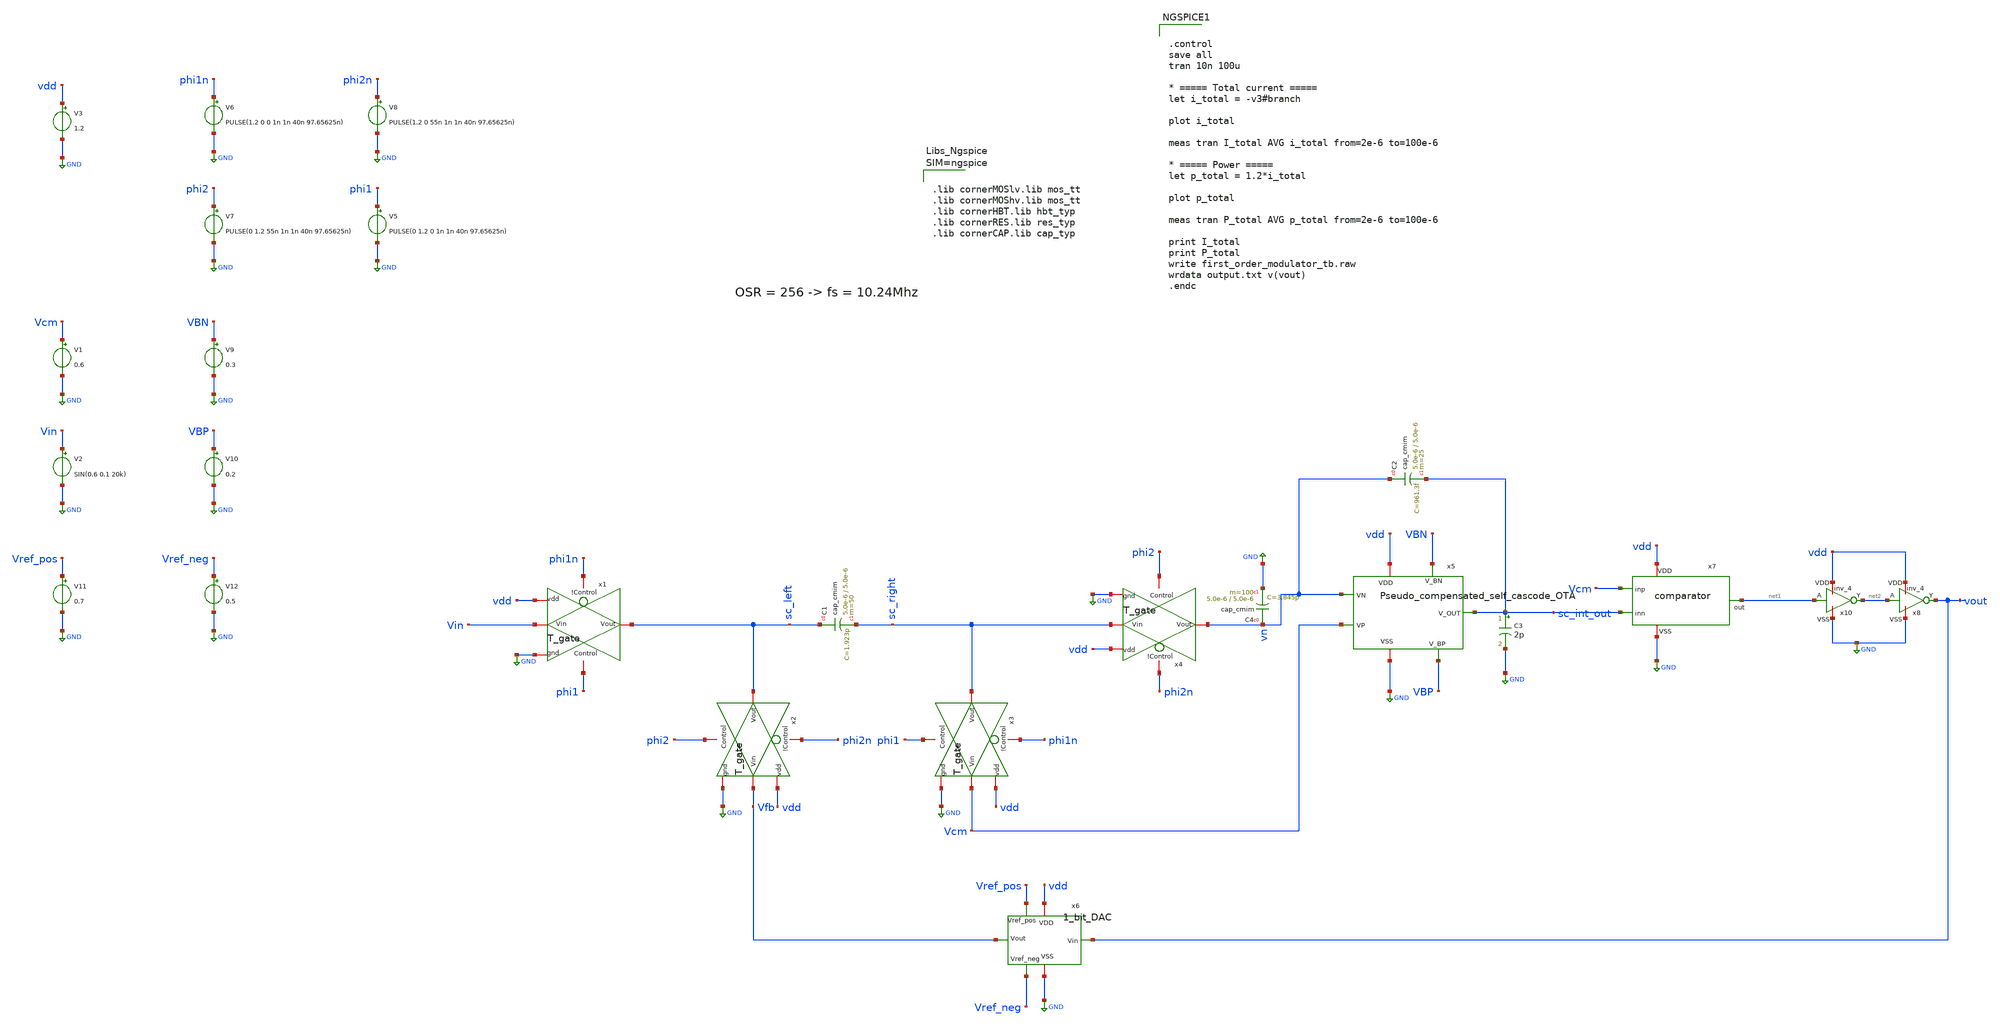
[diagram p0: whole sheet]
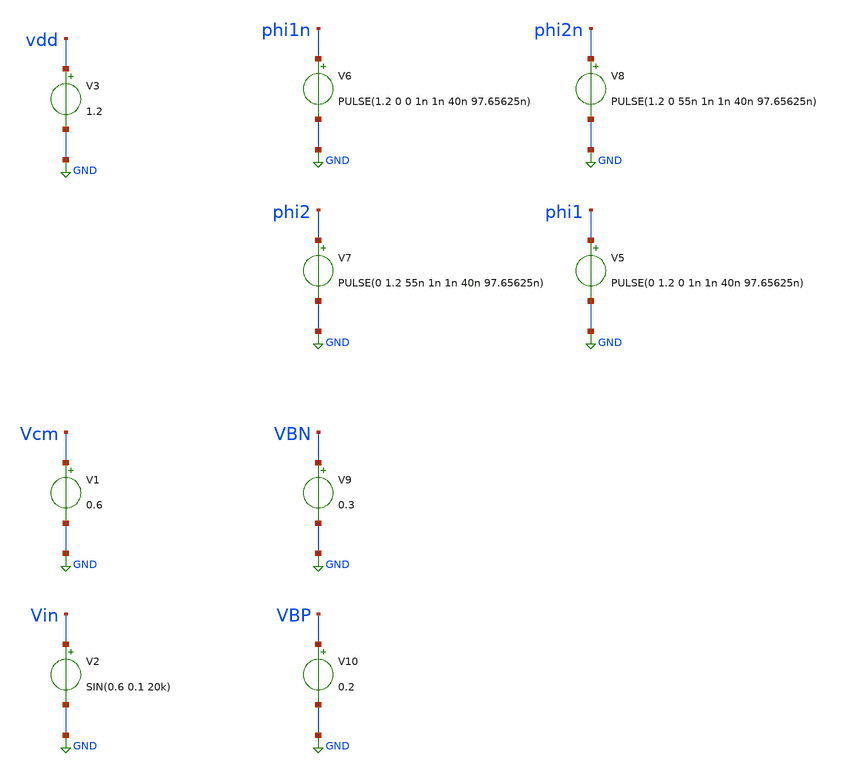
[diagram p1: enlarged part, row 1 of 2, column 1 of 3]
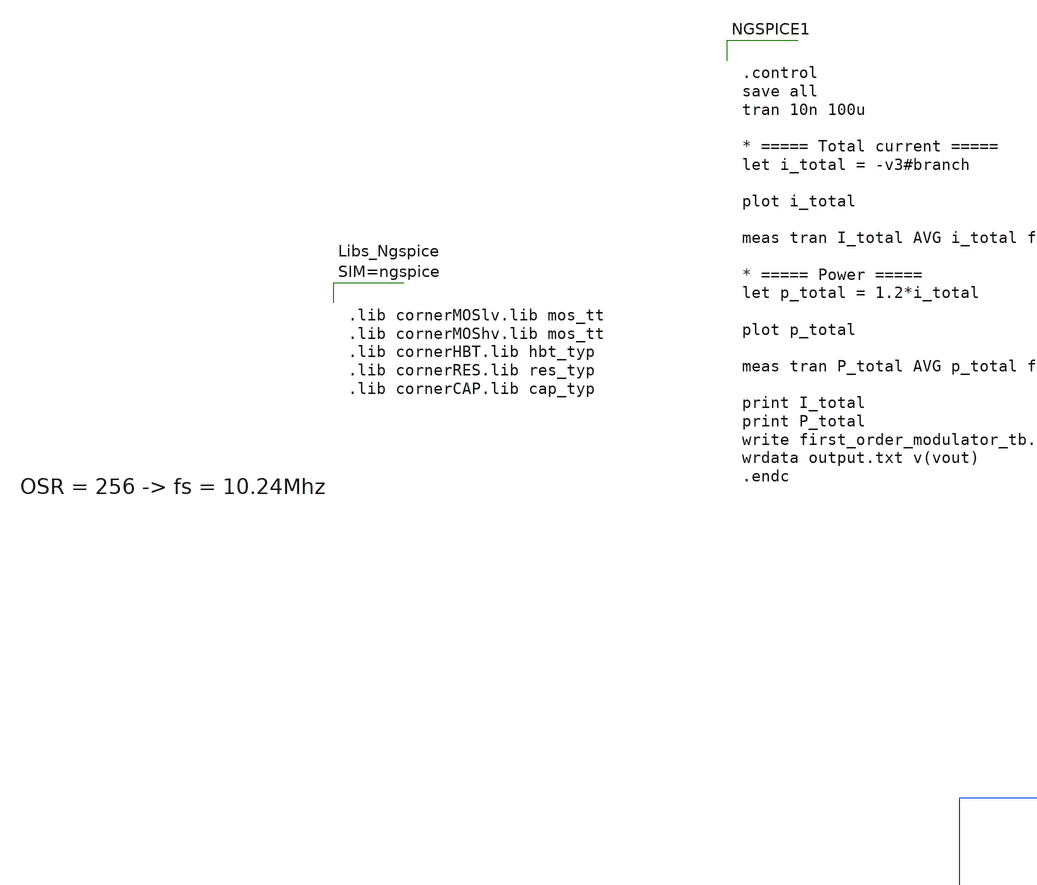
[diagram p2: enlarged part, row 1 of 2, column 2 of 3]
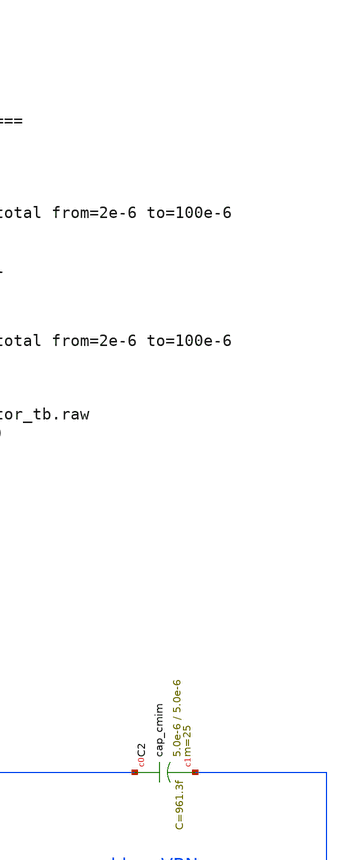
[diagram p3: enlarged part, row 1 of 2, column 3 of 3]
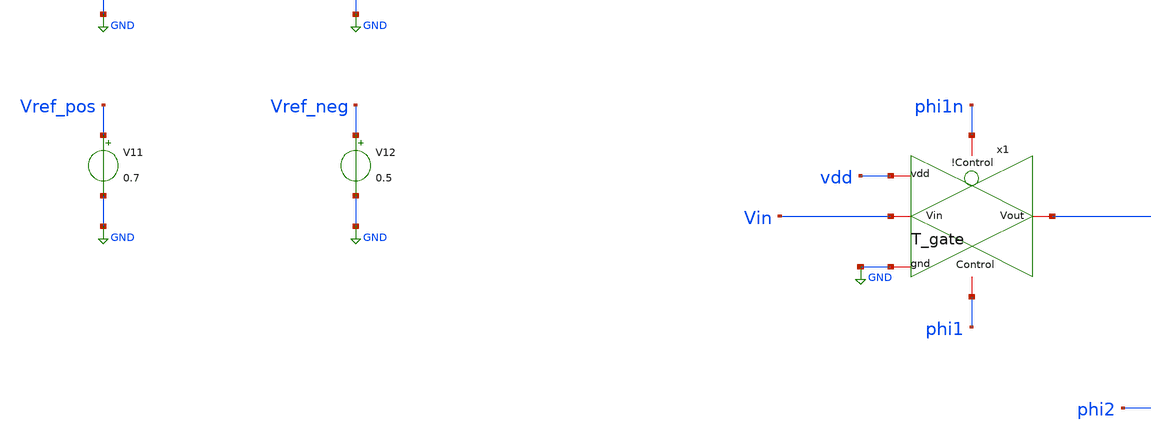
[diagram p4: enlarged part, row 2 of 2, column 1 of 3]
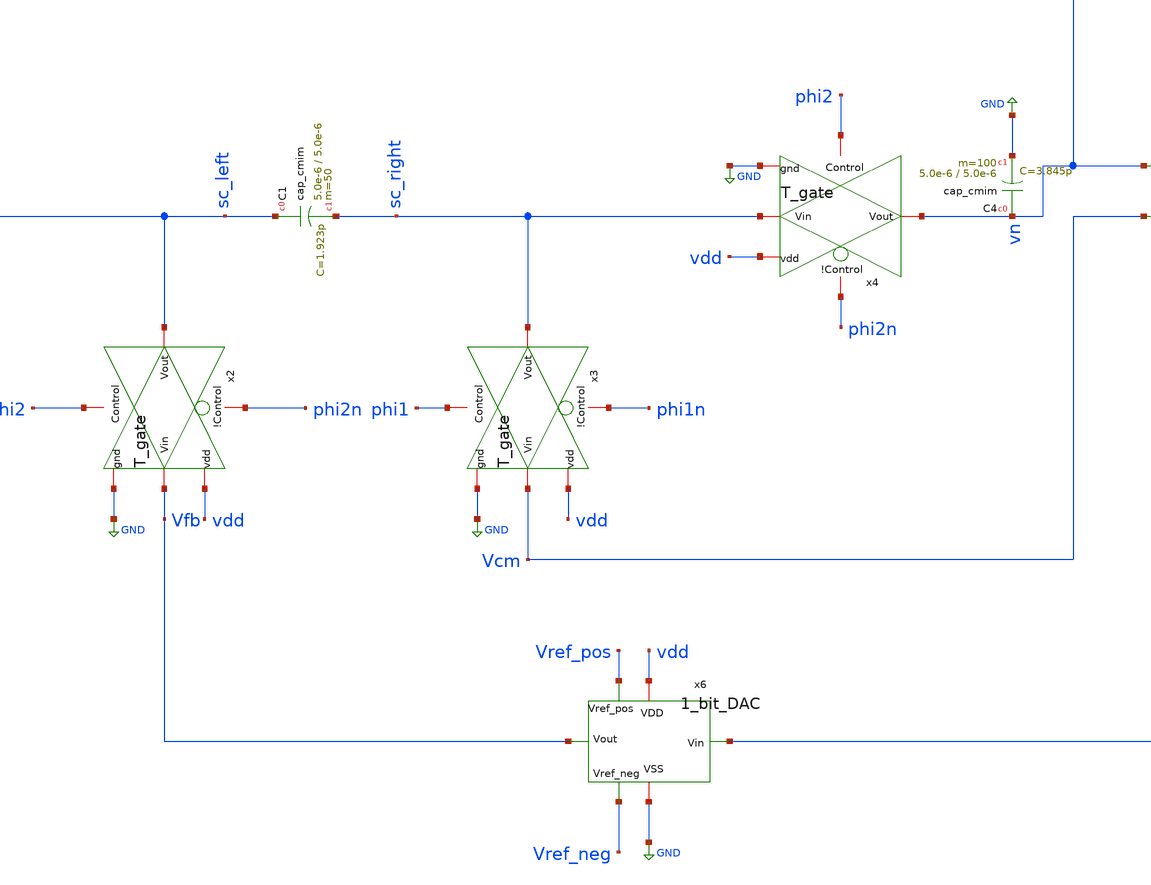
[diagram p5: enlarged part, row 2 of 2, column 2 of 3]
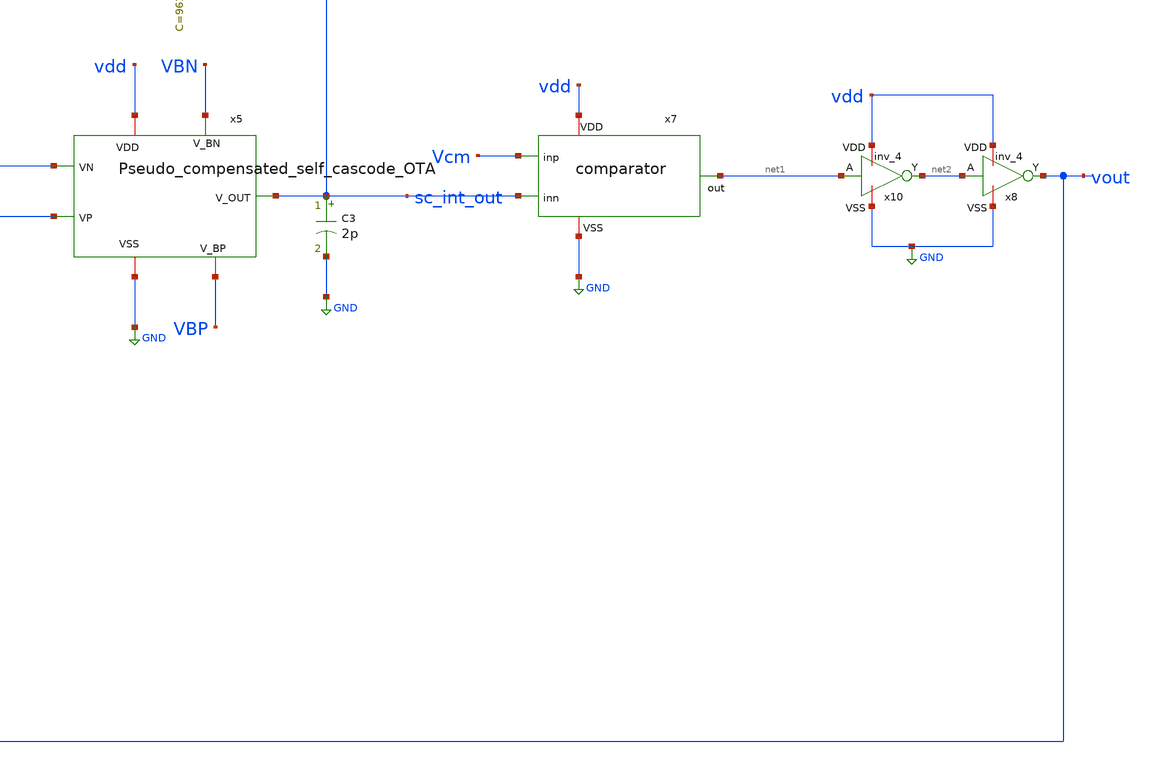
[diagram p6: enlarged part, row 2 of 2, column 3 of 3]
** sch_path: xschem/first_order_modulator_tb.sch
**.subckt first_order_modulator_tb
V5 phi1 GND PULSE(0 1.2 0 1n 1n 40n 97.65625n)
V6 phi1n GND PULSE(1.2 0 0 1n 1n 40n 97.65625n)
V7 phi2 GND PULSE(0 1.2 55n 1n 1n 40n 97.65625n)
V8 phi2n GND PULSE(1.2 0 55n 1n 1n 40n 97.65625n)
V1 Vcm GND 0.6
V2 Vin GND SIN(0.6 0.1 20k)
V3 vdd GND 1.2
V9 VBN GND 0.3
V10 VBP GND 0.2
V12 Vref_neg GND 0.5
V11 Vref_pos GND 0.7
x1 phi1n Vin sc_left GND phi1 vdd T_gate
x2 phi2n Vfb sc_left GND phi2 vdd T_gate
x3 phi1n Vcm sc_right GND phi1 vdd T_gate
XC1 sc_left sc_right cap_cmim w=5.0e-6 l=5.0e-6 m=50 mm_ok=1
x4 phi2n sc_right vn GND phi2 vdd T_gate
XC4 vn GND cap_cmim w=5.0e-6 l=5.0e-6 m=100 mm_ok=1
x5 vn Vcm VBN VBP sc_int_out vdd GND Pseudo_compensated_self_cascode_OTA
C3 sc_int_out GND 2p m=1
x6 vout Vref_pos Vref_neg vdd Vfb GND 1_bit_DAC
XC2 vn sc_int_out cap_cmim w=5.0e-6 l=5.0e-6 m=25 mm_ok=1
x7 vdd net1 sc_int_out Vcm GND comparator
x10 vdd GND net1 net2 inv_4
x8 vdd GND net2 vout inv_4
**** begin user architecture code



.lib cornerMOSlv.lib mos_tt
.lib cornerMOShv.lib mos_tt
.lib cornerHBT.lib hbt_typ
.lib cornerRES.lib res_typ
.lib cornerCAP.lib cap_typ





.control
save all
tran 10n 100u

* ===== Total current =====
let i_total = -v3#branch

plot i_total

meas tran I_total AVG i_total from=2e-6 to=100e-6

* ===== Power =====
let p_total = 1.2*i_total

plot p_total

meas tran P_total AVG p_total from=2e-6 to=100e-6

print I_total
print P_total
write first_order_modulator_tb.raw
wrdata output.txt v(vout)
.endc


**** end user architecture code
**.ends
.GLOBAL GND
.end
